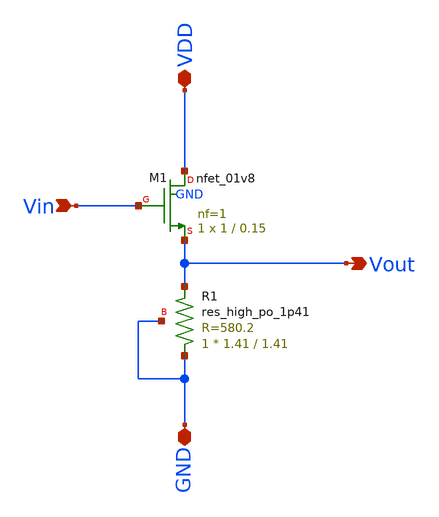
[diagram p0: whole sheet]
** sch_path: src/analog_source_files/source_follower.sch
**.subckt source_follower VDD GND Vin Vout
*.iopin VDD
*.iopin GND
*.ipin Vin
*.opin Vout
XR1 GND Vout GND sky130_fd_pr__res_high_po_1p41 L=1.41 mult=1 m=1
XM1 VDD Vin Vout GND sky130_fd_pr__nfet_01v8 L=0.15 W=1 nf=1 ad='int((1 + 1)/2) * 1 / 1 * 0.29' as='int((1 + 2)/2) * 1 / 1 * 0.29'
+ pd='2*int((1 + 1)/2) * (1 / 1 + 0.29)' ps='2*int((1 + 2)/2) * (1 / 1 + 0.29)' nrd='0.29 / 1 ' nrs='0.29 / 1 '
+ sa=0 sb=0 sd=0 mult=1 m=1
**.ends
.end
